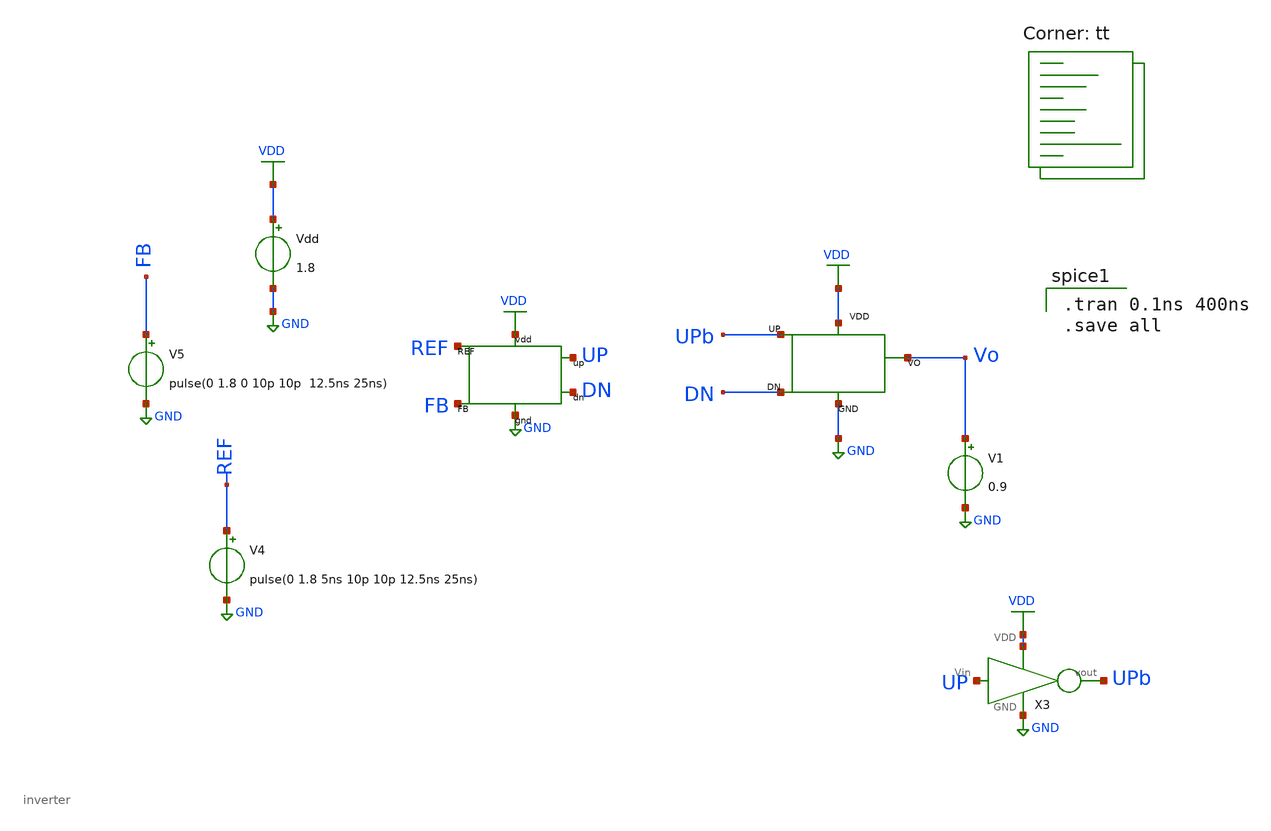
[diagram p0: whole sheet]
** sch_path: pll/pfd_cp_lf_lib/PFD_CP_tb/xschem/PFD_CP_tb.sch
**.subckt PFD_CP_tb
Vdd VDD GND 1.8
X2 REF UP FB VDD GND DN PFD
V4 REF GND pulse(0 1.8 5ns 10p 10p 12.5ns 25ns)
V5 FB GND pulse(0 1.8 0 10p 10p 12.5ns 25ns)
V1 Vo GND 0.9
X3 UP UPb VDD GND inverter
X1 DN UPb Vo GND VDD CP
**** begin user architecture code
.lib $::SKYWATER_MODELS/sky130.lib.spice tt

.tran 0.1ns 400ns
.save all

**** end user architecture code
**.ends
.GLOBAL GND
.GLOBAL VDD
.end
